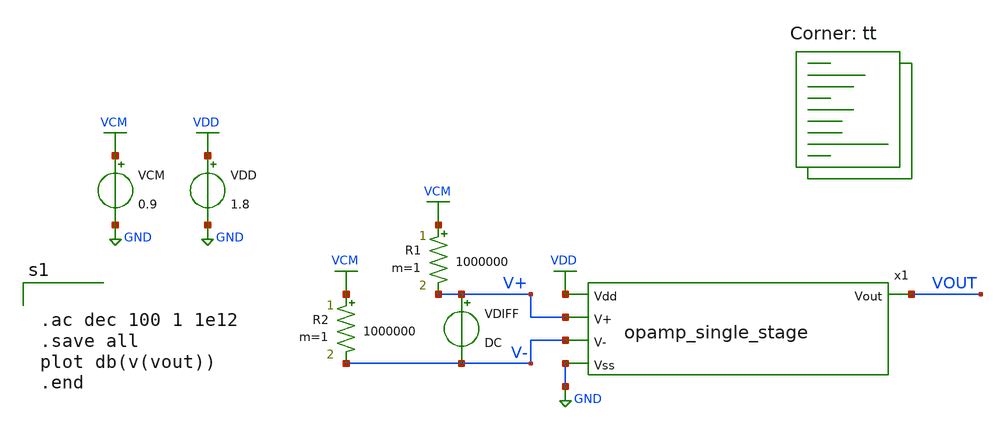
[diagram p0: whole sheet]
** sch_path: analog/schematics/tb_ac_analysis.sch
**.subckt tb_ac_analysis
VDD VDD GND 1.8
VCM VCM GND 0.9
R1 VCM V+ 1000000 m=1
VDIFF V+ V- DC
R2 VCM V- 1000000 m=1
x1 VDD VOUT V+ V- GND opamp_single_stage
**** begin user architecture code


.ac dec 100 1 1e12
.save all
plot db(v(vout))
.end


.lib $::SKYWATER_MODELS/sky130.lib.spice tt
**** end user architecture code
**.ends

* expanding   symbol:  opamp_single_stage.sym # of pins=5
** sym_path: analog/schematics/opamp_single_stage.sym
** sch_path: analog/schematics/opamp_single_stage.sch
.subckt opamp_single_stage Vdd Vout V+ V- Vss
*.opin Vout
*.ipin Vdd
*.ipin Vss
*.ipin V+
*.ipin V-
XM3 net1 V+ net2 Vss sky130_fd_pr__nfet_01v8 L=0.25 W=1 nf=1 ad='int((nf+1)/2) * W/nf * 0.29' as='int((nf+2)/2) * W/nf * 0.29'
+ pd='2*int((nf+1)/2) * (W/nf + 0.29)' ps='2*int((nf+2)/2) * (W/nf + 0.29)' nrd='0.29 / W' nrs='0.29 / W'
+ sa=0 sb=0 sd=0 mult=1 m=1
XM4 Vout V- net2 Vss sky130_fd_pr__nfet_01v8 L=0.25 W=1 nf=1 ad='int((nf+1)/2) * W/nf * 0.29' as='int((nf+2)/2) * W/nf * 0.29'
+ pd='2*int((nf+1)/2) * (W/nf + 0.29)' ps='2*int((nf+2)/2) * (W/nf + 0.29)' nrd='0.29 / W' nrs='0.29 / W'
+ sa=0 sb=0 sd=0 mult=1 m=1
XM5 net2 net3 Vss Vss sky130_fd_pr__nfet_01v8 L=0.25 W=1 nf=1 ad='int((nf+1)/2) * W/nf * 0.29' as='int((nf+2)/2) * W/nf * 0.29'
+ pd='2*int((nf+1)/2) * (W/nf + 0.29)' ps='2*int((nf+2)/2) * (W/nf + 0.29)' nrd='0.29 / W' nrs='0.29 / W'
+ sa=0 sb=0 sd=0 mult=1 m=1
XM1 net1 net1 Vdd Vdd sky130_fd_pr__pfet_01v8 L=0.25 W=1 nf=1 ad='int((nf+1)/2) * W/nf * 0.29' as='int((nf+2)/2) * W/nf * 0.29'
+ pd='2*int((nf+1)/2) * (W/nf + 0.29)' ps='2*int((nf+2)/2) * (W/nf + 0.29)' nrd='0.29 / W' nrs='0.29 / W'
+ sa=0 sb=0 sd=0 mult=1 m=1
XM2 Vout net1 Vdd Vdd sky130_fd_pr__pfet_01v8 L=0.25 W=1 nf=1 ad='int((nf+1)/2) * W/nf * 0.29' as='int((nf+2)/2) * W/nf * 0.29'
+ pd='2*int((nf+1)/2) * (W/nf + 0.29)' ps='2*int((nf+2)/2) * (W/nf + 0.29)' nrd='0.29 / W' nrs='0.29 / W'
+ sa=0 sb=0 sd=0 mult=1 m=1
XM6 net3 net3 Vss Vss sky130_fd_pr__nfet_01v8 L=0.25 W=1 nf=1 ad='int((nf+1)/2) * W/nf * 0.29' as='int((nf+2)/2) * W/nf * 0.29'
+ pd='2*int((nf+1)/2) * (W/nf + 0.29)' ps='2*int((nf+2)/2) * (W/nf + 0.29)' nrd='0.29 / W' nrs='0.29 / W'
+ sa=0 sb=0 sd=0 mult=1 m=1
XR1 net3 Vdd net4 sky130_fd_pr__res_high_po W=2.5 L=0.1 mult=1 m=1
.ends

.GLOBAL GND
.GLOBAL VDD
.GLOBAL VCM
.end
